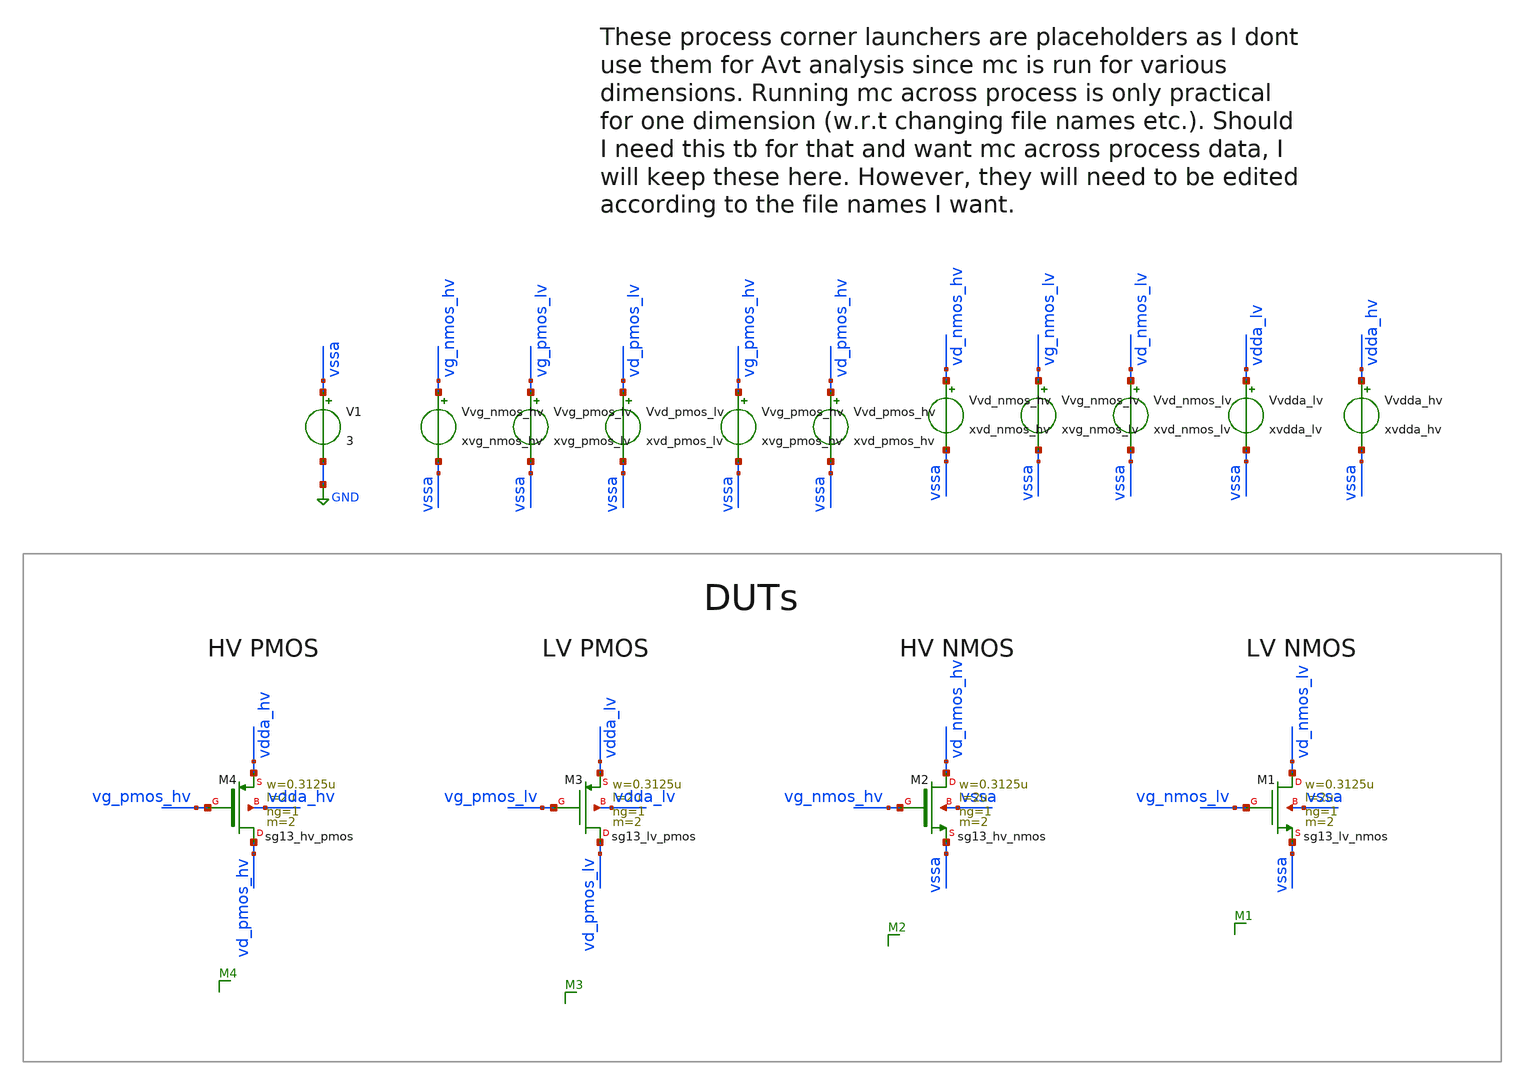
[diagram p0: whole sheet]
** sch_path: tb_vth_ihp/tb_vth_mc_ihp.sch
**.subckt tb_vth_mc_ihp
XM1 vd_nmos_lv vg_nmos_lv vssa vssa sg13_lv_nmos w=0.3125u l=2u ng=1 m=2 mm_ok=1
V1 vssa GND 3
Vvg_nmos_lv vg_nmos_lv vssa xvg_nmos_lv
Vvd_nmos_lv vd_nmos_lv vssa xvd_nmos_lv
XM2 vd_nmos_hv vg_nmos_hv vssa vssa sg13_hv_nmos w=0.3125u l=2u ng=1 m=2 mm_ok=1
Vvdda_lv vdda_lv vssa xvdda_lv
Vvdda_hv vdda_hv vssa xvdda_hv
XM3 vd_pmos_lv vg_pmos_lv vdda_lv vdda_lv sg13_lv_pmos w=0.3125u l=2u ng=1 m=2 mm_ok=1
Vvg_pmos_lv vg_pmos_lv vssa xvg_pmos_lv
Vvd_pmos_lv vd_pmos_lv vssa xvd_pmos_lv
Vvg_pmos_hv vg_pmos_hv vssa xvg_pmos_hv
Vvd_pmos_hv vd_pmos_hv vssa xvd_pmos_hv
XM4 vd_pmos_hv vg_pmos_hv vdda_hv vdda_hv sg13_hv_pmos w=0.3125u l=2u ng=1 m=2 mm_ok=1
Vvg_nmos_hv vg_nmos_hv vssa xvg_nmos_hv
Vvd_nmos_hv vd_nmos_hv vssa xvd_nmos_hv
**** begin user architecture code

** opencircuitdesign pdks install
.lib /home/slice/pdk/iHP/IHP-Open-PDK/ihp-sg13g2/libs.tech/ngspice/models/cornerMOSlv.lib mos_tt_mismatch
.lib /home/slice/pdk/iHP/IHP-Open-PDK/ihp-sg13g2/libs.tech/ngspice/models/cornerMOShv.lib mos_tt_mismatch
*.lib /home/slice/pdk/iHP/IHP-Open-PDK/ihp-sg13g2/libs.tech/ngspice/models/cornerMOSlv.lib mos_tt_stat
*.lib /home/slice/pdk/iHP/IHP-Open-PDK/ihp-sg13g2/libs.tech/ngspice/models/cornerMOShv.lib mos_tt_stat
.lib /home/slice/pdk/iHP/IHP-Open-PDK/ihp-sg13g2/libs.tech/ngspice/models/cornerRES.lib res_typ
.include /home/slice/pdk/iHP/IHP-Open-PDK/ihp-sg13g2/libs.tech/ngspice/models/diodes.lib


* Parameters
.param xvg_nmos_lv = 0.4
.param xvd_nmos_lv = 0.35
.param xvg_nmos_hv = 0.79
.param xvd_nmos_hv = 0.35
.param xvdda_hv = 3.3
.csparam xvdda_hv_var = 'xvdda_hv'
.param xvdda_lv = 1.65
.csparam xvdda_lv_var = 'xvdda_lv'
.param xvg_pmos_lv = 1.1
.param xvg_pmos_hv = 2.414
.param xvd_pmos_lv = 1.3
.param xvd_pmos_hv = 2.95
.param xtsim = 5u
.csparam xtsim_var = 'xtsim'
.param xstep_en = 1
.temp 27


  ** must save the below for DCOP analysis to be back annotated onto the schematic
  .option savecurrents

  .include tb_vth_mc_ihp.save

  .save v(vd_nmos) v(vg_nmos)
  .save @n.xm1.nsg13_lv_nmos[ids] @n.xm2.nsg13_hv_nmos[ids] @n.xm3.nsg13_lv_pmos[ids] @n.xm4.nsg13_hv_pmos[ids]

  .control

    let run = 1

    dowhile run <= 100
    reset

** 1. DCOP ANALYSIS **

  op

  let vth_meas_nmoslv = @n.xm1.nsg13_lv_nmos[vth]
  echo "$&vth_meas_nmoslv" >> vth_measures_nmoslv_tt_mc.txt
  let vth_meas_nmoshv = @n.xm2.nsg13_hv_nmos[vth]
  echo "$&vth_meas_nmoshv" >> vth_measures_nmoshv_tt_mc.txt
  let vth_meas_pmoslv = @n.xm3.nsg13_lv_pmos[vth]
  echo "$&vth_meas_pmoslv" >> vth_measures_pmoslv_tt_mc.txt
  let vth_meas_pmoshv = @n.xm4.nsg13_hv_pmos[vth]
  echo "$&vth_meas_pmoshv" >> vth_measures_pmoshv_tt_mc.txt

    remzerovec
    set filetype=binary
    ** first write deletes existing file
    write tb_vth_mc_ihp.raw
    ** set appendwrite appends following writes to existing raw file
    set appendwrite
    let run = run+1

    end

  setplot

quit 0
.endc




**** end user architecture code
**.ends
.GLOBAL GND
.end
